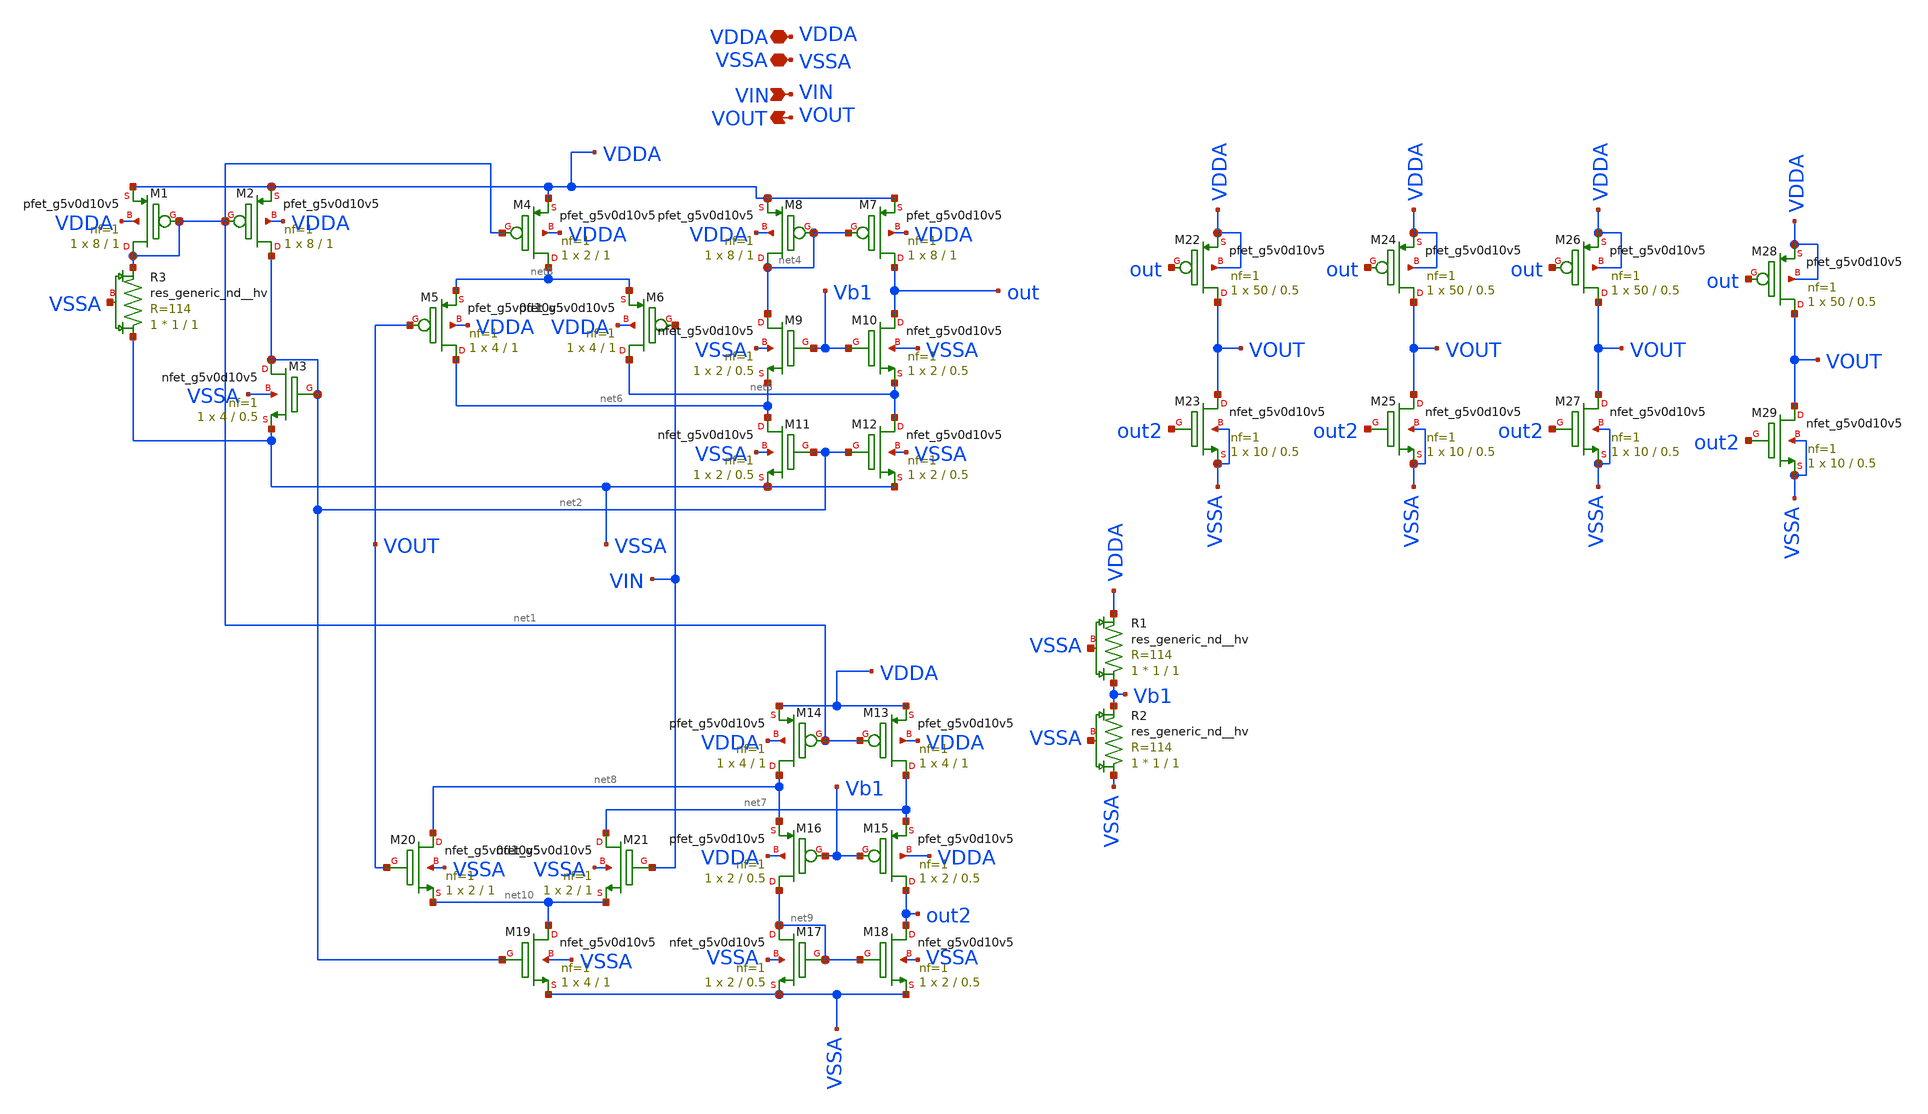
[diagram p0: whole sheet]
** sch_path: Rail_Rail_opamp_3v3/Schematic_mismatch_montecarlo/opamp.sch
**.subckt opamp VOUT VIN VSSA VDDA
*.opin VOUT
*.ipin VIN
*.iopin VSSA
*.iopin VDDA
XM1 net1 net1 VDDA VDDA sky130_fd_pr__pfet_g5v0d10v5 L=1 W=8 nf=1 ad='int((nf+1)/2) * W/nf * 0.29' as='int((nf+2)/2) * W/nf * 0.29'
+ pd='2*int((nf+1)/2) * (W/nf + 0.29)' ps='2*int((nf+2)/2) * (W/nf + 0.29)' nrd='0.29 / W' nrs='0.29 / W'
+ sa=0 sb=0 sd=0 mult=1 m=1
XM2 net2 net1 VDDA VDDA sky130_fd_pr__pfet_g5v0d10v5 L=1 W=8 nf=1 ad='int((nf+1)/2) * W/nf * 0.29' as='int((nf+2)/2) * W/nf * 0.29'
+ pd='2*int((nf+1)/2) * (W/nf + 0.29)' ps='2*int((nf+2)/2) * (W/nf + 0.29)' nrd='0.29 / W' nrs='0.29 / W'
+ sa=0 sb=0 sd=0 mult=1 m=1
XM3 net2 net2 VSSA VSSA sky130_fd_pr__nfet_g5v0d10v5 L=0.5 W=4 nf=1 ad='int((nf+1)/2) * W/nf * 0.29'
+ as='int((nf+2)/2) * W/nf * 0.29' pd='2*int((nf+1)/2) * (W/nf + 0.29)' ps='2*int((nf+2)/2) * (W/nf + 0.29)'
+ nrd='0.29 / W' nrs='0.29 / W' sa=0 sb=0 sd=0 mult=1 m=1
XM4 net3 net1 VDDA VDDA sky130_fd_pr__pfet_g5v0d10v5 L=1 W=2 nf=1 ad='int((nf+1)/2) * W/nf * 0.29' as='int((nf+2)/2) * W/nf * 0.29'
+ pd='2*int((nf+1)/2) * (W/nf + 0.29)' ps='2*int((nf+2)/2) * (W/nf + 0.29)' nrd='0.29 / W' nrs='0.29 / W'
+ sa=0 sb=0 sd=0 mult=1 m=1
XM5 net6 VOUT net3 VDDA sky130_fd_pr__pfet_g5v0d10v5 L=1 W=4 nf=1 ad='int((nf+1)/2) * W/nf * 0.29' as='int((nf+2)/2) * W/nf * 0.29'
+ pd='2*int((nf+1)/2) * (W/nf + 0.29)' ps='2*int((nf+2)/2) * (W/nf + 0.29)' nrd='0.29 / W' nrs='0.29 / W'
+ sa=0 sb=0 sd=0 mult=1 m=1
XM6 net5 VIN net3 VDDA sky130_fd_pr__pfet_g5v0d10v5 L=1 W=4 nf=1 ad='int((nf+1)/2) * W/nf * 0.29' as='int((nf+2)/2) * W/nf * 0.29'
+ pd='2*int((nf+1)/2) * (W/nf + 0.29)' ps='2*int((nf+2)/2) * (W/nf + 0.29)' nrd='0.29 / W' nrs='0.29 / W'
+ sa=0 sb=0 sd=0 mult=1 m=1
XM7 out net4 VDDA VDDA sky130_fd_pr__pfet_g5v0d10v5 L=1 W=8 nf=1 ad='int((nf+1)/2) * W/nf * 0.29' as='int((nf+2)/2) * W/nf * 0.29'
+ pd='2*int((nf+1)/2) * (W/nf + 0.29)' ps='2*int((nf+2)/2) * (W/nf + 0.29)' nrd='0.29 / W' nrs='0.29 / W'
+ sa=0 sb=0 sd=0 mult=1 m=1
XM8 net4 net4 VDDA VDDA sky130_fd_pr__pfet_g5v0d10v5 L=1 W=8 nf=1 ad='int((nf+1)/2) * W/nf * 0.29' as='int((nf+2)/2) * W/nf * 0.29'
+ pd='2*int((nf+1)/2) * (W/nf + 0.29)' ps='2*int((nf+2)/2) * (W/nf + 0.29)' nrd='0.29 / W' nrs='0.29 / W'
+ sa=0 sb=0 sd=0 mult=1 m=1
XM9 net4 Vb1 net6 VSSA sky130_fd_pr__nfet_g5v0d10v5 L=0.5 W=2 nf=1 ad='int((nf+1)/2) * W/nf * 0.29' as='int((nf+2)/2) * W/nf * 0.29'
+ pd='2*int((nf+1)/2) * (W/nf + 0.29)' ps='2*int((nf+2)/2) * (W/nf + 0.29)' nrd='0.29 / W' nrs='0.29 / W'
+ sa=0 sb=0 sd=0 mult=1 m=1
XM10 out Vb1 net5 VSSA sky130_fd_pr__nfet_g5v0d10v5 L=0.5 W=2 nf=1 ad='int((nf+1)/2) * W/nf * 0.29' as='int((nf+2)/2) * W/nf * 0.29'
+ pd='2*int((nf+1)/2) * (W/nf + 0.29)' ps='2*int((nf+2)/2) * (W/nf + 0.29)' nrd='0.29 / W' nrs='0.29 / W'
+ sa=0 sb=0 sd=0 mult=1 m=1
XM11 net6 net2 VSSA VSSA sky130_fd_pr__nfet_g5v0d10v5 L=0.5 W=2 nf=1 ad='int((nf+1)/2) * W/nf * 0.29'
+ as='int((nf+2)/2) * W/nf * 0.29' pd='2*int((nf+1)/2) * (W/nf + 0.29)' ps='2*int((nf+2)/2) * (W/nf + 0.29)'
+ nrd='0.29 / W' nrs='0.29 / W' sa=0 sb=0 sd=0 mult=1 m=1
XM12 net5 net2 VSSA VSSA sky130_fd_pr__nfet_g5v0d10v5 L=0.5 W=2 nf=1 ad='int((nf+1)/2) * W/nf * 0.29'
+ as='int((nf+2)/2) * W/nf * 0.29' pd='2*int((nf+1)/2) * (W/nf + 0.29)' ps='2*int((nf+2)/2) * (W/nf + 0.29)'
+ nrd='0.29 / W' nrs='0.29 / W' sa=0 sb=0 sd=0 mult=1 m=1
XM13 net7 net1 VDDA VDDA sky130_fd_pr__pfet_g5v0d10v5 L=1 W=4 nf=1 ad='int((nf+1)/2) * W/nf * 0.29' as='int((nf+2)/2) * W/nf * 0.29'
+ pd='2*int((nf+1)/2) * (W/nf + 0.29)' ps='2*int((nf+2)/2) * (W/nf + 0.29)' nrd='0.29 / W' nrs='0.29 / W'
+ sa=0 sb=0 sd=0 mult=1 m=1
XM14 net8 net1 VDDA VDDA sky130_fd_pr__pfet_g5v0d10v5 L=1 W=4 nf=1 ad='int((nf+1)/2) * W/nf * 0.29' as='int((nf+2)/2) * W/nf * 0.29'
+ pd='2*int((nf+1)/2) * (W/nf + 0.29)' ps='2*int((nf+2)/2) * (W/nf + 0.29)' nrd='0.29 / W' nrs='0.29 / W'
+ sa=0 sb=0 sd=0 mult=1 m=1
XM17 net9 net9 VSSA VSSA sky130_fd_pr__nfet_g5v0d10v5 L=0.5 W=2 nf=1 ad='int((nf+1)/2) * W/nf * 0.29'
+ as='int((nf+2)/2) * W/nf * 0.29' pd='2*int((nf+1)/2) * (W/nf + 0.29)' ps='2*int((nf+2)/2) * (W/nf + 0.29)'
+ nrd='0.29 / W' nrs='0.29 / W' sa=0 sb=0 sd=0 mult=1 m=1
XM18 out2 net9 VSSA VSSA sky130_fd_pr__nfet_g5v0d10v5 L=0.5 W=2 nf=1 ad='int((nf+1)/2) * W/nf * 0.29'
+ as='int((nf+2)/2) * W/nf * 0.29' pd='2*int((nf+1)/2) * (W/nf + 0.29)' ps='2*int((nf+2)/2) * (W/nf + 0.29)'
+ nrd='0.29 / W' nrs='0.29 / W' sa=0 sb=0 sd=0 mult=1 m=1
XM15 out2 Vb1 net7 VDDA sky130_fd_pr__pfet_g5v0d10v5 L=0.5 W=2 nf=1 ad='int((nf+1)/2) * W/nf * 0.29'
+ as='int((nf+2)/2) * W/nf * 0.29' pd='2*int((nf+1)/2) * (W/nf + 0.29)' ps='2*int((nf+2)/2) * (W/nf + 0.29)'
+ nrd='0.29 / W' nrs='0.29 / W' sa=0 sb=0 sd=0 mult=1 m=1
XM16 net9 Vb1 net8 VDDA sky130_fd_pr__pfet_g5v0d10v5 L=0.5 W=2 nf=1 ad='int((nf+1)/2) * W/nf * 0.29'
+ as='int((nf+2)/2) * W/nf * 0.29' pd='2*int((nf+1)/2) * (W/nf + 0.29)' ps='2*int((nf+2)/2) * (W/nf + 0.29)'
+ nrd='0.29 / W' nrs='0.29 / W' sa=0 sb=0 sd=0 mult=1 m=1
XM19 net10 net2 VSSA VSSA sky130_fd_pr__nfet_g5v0d10v5 L=1 W=4 nf=1 ad='int((nf+1)/2) * W/nf * 0.29'
+ as='int((nf+2)/2) * W/nf * 0.29' pd='2*int((nf+1)/2) * (W/nf + 0.29)' ps='2*int((nf+2)/2) * (W/nf + 0.29)'
+ nrd='0.29 / W' nrs='0.29 / W' sa=0 sb=0 sd=0 mult=1 m=1
XM20 net8 VOUT net10 VSSA sky130_fd_pr__nfet_g5v0d10v5 L=1 W=2 nf=1 ad='int((nf+1)/2) * W/nf * 0.29'
+ as='int((nf+2)/2) * W/nf * 0.29' pd='2*int((nf+1)/2) * (W/nf + 0.29)' ps='2*int((nf+2)/2) * (W/nf + 0.29)'
+ nrd='0.29 / W' nrs='0.29 / W' sa=0 sb=0 sd=0 mult=1 m=1
XM21 net7 VIN net10 VSSA sky130_fd_pr__nfet_g5v0d10v5 L=1 W=2 nf=1 ad='int((nf+1)/2) * W/nf * 0.29' as='int((nf+2)/2) * W/nf * 0.29'
+ pd='2*int((nf+1)/2) * (W/nf + 0.29)' ps='2*int((nf+2)/2) * (W/nf + 0.29)' nrd='0.29 / W' nrs='0.29 / W'
+ sa=0 sb=0 sd=0 mult=1 m=1
XM22 VOUT out VDDA VDDA sky130_fd_pr__pfet_g5v0d10v5 L=0.5 W=50 nf=1 ad='int((nf+1)/2) * W/nf * 0.29'
+ as='int((nf+2)/2) * W/nf * 0.29' pd='2*int((nf+1)/2) * (W/nf + 0.29)' ps='2*int((nf+2)/2) * (W/nf + 0.29)'
+ nrd='0.29 / W' nrs='0.29 / W' sa=0 sb=0 sd=0 mult=1 m=1
XM23 VOUT out2 VSSA VSSA sky130_fd_pr__nfet_g5v0d10v5 L=0.5 W=10 nf=1 ad='int((nf+1)/2) * W/nf * 0.29'
+ as='int((nf+2)/2) * W/nf * 0.29' pd='2*int((nf+1)/2) * (W/nf + 0.29)' ps='2*int((nf+2)/2) * (W/nf + 0.29)'
+ nrd='0.29 / W' nrs='0.29 / W' sa=0 sb=0 sd=0 mult=1 m=1
XR3 VSSA net1 VSSA sky130_fd_pr__res_generic_nd__hv W=1 L=1 mult=1 m=1
XR1 Vb1 VDDA VSSA sky130_fd_pr__res_generic_nd__hv W=1 L=1 mult=1 m=1
XR2 VSSA Vb1 VSSA sky130_fd_pr__res_generic_nd__hv W=1 L=1 mult=1 m=1
XM24 VOUT out VDDA VDDA sky130_fd_pr__pfet_g5v0d10v5 L=0.5 W=50 nf=1 ad='int((nf+1)/2) * W/nf * 0.29'
+ as='int((nf+2)/2) * W/nf * 0.29' pd='2*int((nf+1)/2) * (W/nf + 0.29)' ps='2*int((nf+2)/2) * (W/nf + 0.29)'
+ nrd='0.29 / W' nrs='0.29 / W' sa=0 sb=0 sd=0 mult=1 m=1
XM25 VOUT out2 VSSA VSSA sky130_fd_pr__nfet_g5v0d10v5 L=0.5 W=10 nf=1 ad='int((nf+1)/2) * W/nf * 0.29'
+ as='int((nf+2)/2) * W/nf * 0.29' pd='2*int((nf+1)/2) * (W/nf + 0.29)' ps='2*int((nf+2)/2) * (W/nf + 0.29)'
+ nrd='0.29 / W' nrs='0.29 / W' sa=0 sb=0 sd=0 mult=1 m=1
XM26 VOUT out VDDA VDDA sky130_fd_pr__pfet_g5v0d10v5 L=0.5 W=50 nf=1 ad='int((nf+1)/2) * W/nf * 0.29'
+ as='int((nf+2)/2) * W/nf * 0.29' pd='2*int((nf+1)/2) * (W/nf + 0.29)' ps='2*int((nf+2)/2) * (W/nf + 0.29)'
+ nrd='0.29 / W' nrs='0.29 / W' sa=0 sb=0 sd=0 mult=1 m=1
XM27 VOUT out2 VSSA VSSA sky130_fd_pr__nfet_g5v0d10v5 L=0.5 W=10 nf=1 ad='int((nf+1)/2) * W/nf * 0.29'
+ as='int((nf+2)/2) * W/nf * 0.29' pd='2*int((nf+1)/2) * (W/nf + 0.29)' ps='2*int((nf+2)/2) * (W/nf + 0.29)'
+ nrd='0.29 / W' nrs='0.29 / W' sa=0 sb=0 sd=0 mult=1 m=1
XM28 VOUT out VDDA VDDA sky130_fd_pr__pfet_g5v0d10v5 L=0.5 W=50 nf=1 ad='int((nf+1)/2) * W/nf * 0.29'
+ as='int((nf+2)/2) * W/nf * 0.29' pd='2*int((nf+1)/2) * (W/nf + 0.29)' ps='2*int((nf+2)/2) * (W/nf + 0.29)'
+ nrd='0.29 / W' nrs='0.29 / W' sa=0 sb=0 sd=0 mult=1 m=1
XM29 VOUT out2 VSSA VSSA sky130_fd_pr__nfet_g5v0d10v5 L=0.5 W=10 nf=1 ad='int((nf+1)/2) * W/nf * 0.29'
+ as='int((nf+2)/2) * W/nf * 0.29' pd='2*int((nf+1)/2) * (W/nf + 0.29)' ps='2*int((nf+2)/2) * (W/nf + 0.29)'
+ nrd='0.29 / W' nrs='0.29 / W' sa=0 sb=0 sd=0 mult=1 m=1
**.ends
.end
